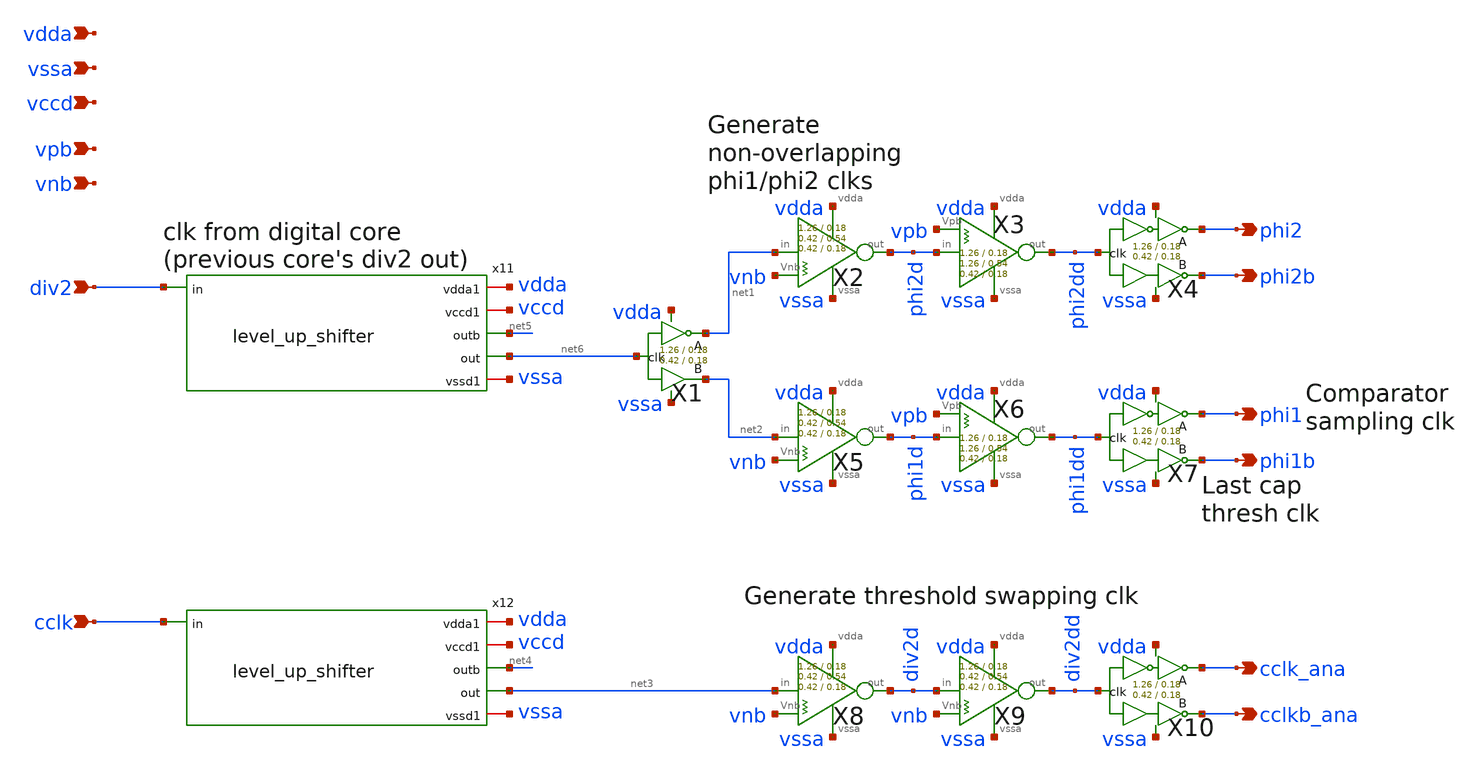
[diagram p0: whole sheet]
** sch_path: xschem/clkgen/filter_clkgen.sch
**.subckt filter_clkgen div2 phi2 phi2b phi1 phi1b cclk_ana cclkb_ana vpb vnb vdda vssa cclk vccd
*.ipin div2
*.opin phi2
*.opin phi2b
*.opin phi1
*.opin phi1b
*.opin cclk_ana
*.opin cclkb_ana
*.ipin vpb
*.ipin vnb
*.ipin vdda
*.ipin vssa
*.ipin cclk
*.ipin vccd
X4 phi2dd phi2 phi2b vdda vssa comp_clks Wpmos=1.26 Lpmos=0.18 Wnmos=0.42 Lnmos=0.18
X7 phi1dd phi1 phi1b vdda vssa comp_clks Wpmos=1.26 Lpmos=0.18 Wnmos=0.42 Lnmos=0.18
X10 div2dd cclk_ana cclkb_ana vdda vssa comp_clks Wpmos=1.26 Lpmos=0.18 Wnmos=0.42 Lnmos=0.18
X1 net6 net1 net2 vdda vssa comp_clks_1stage Wpmos=1.26 Lpmos=0.18 Wnmos=0.42 Lnmos=0.18
X2 net1 phi2d vnb vdda vssa inv_weak_pulldown Wpmos=1.26 Lpmos= Wnmos= Lnmos=0.54
X5 net2 phi1d vnb vdda vssa inv_weak_pulldown Wpmos=1.26 Lpmos= Wnmos= Lnmos=0.54
X8 net3 div2d vnb vdda vssa inv_weak_pulldown Wpmos=1.26 Lpmos= Wnmos= Lnmos=0.54
X9 div2d div2dd vnb vdda vssa inv_weak_pulldown Wpmos=1.26 Lpmos= Wnmos= Lnmos=0.54
X3 phi2d phi2dd vpb vdda vssa inv_weak_pullup Wpmos=1.26 Lpmos=0.54 Wnmos= Lnmos=
X6 phi1d phi1dd vpb vdda vssa inv_weak_pullup Wpmos=1.26 Lpmos=0.54 Wnmos= Lnmos=
x12 vdda vccd cclk net4 net3 vssa level_up_shifter
x11 vdda vccd div2 net5 net6 vssa level_up_shifter
**.ends
.end
